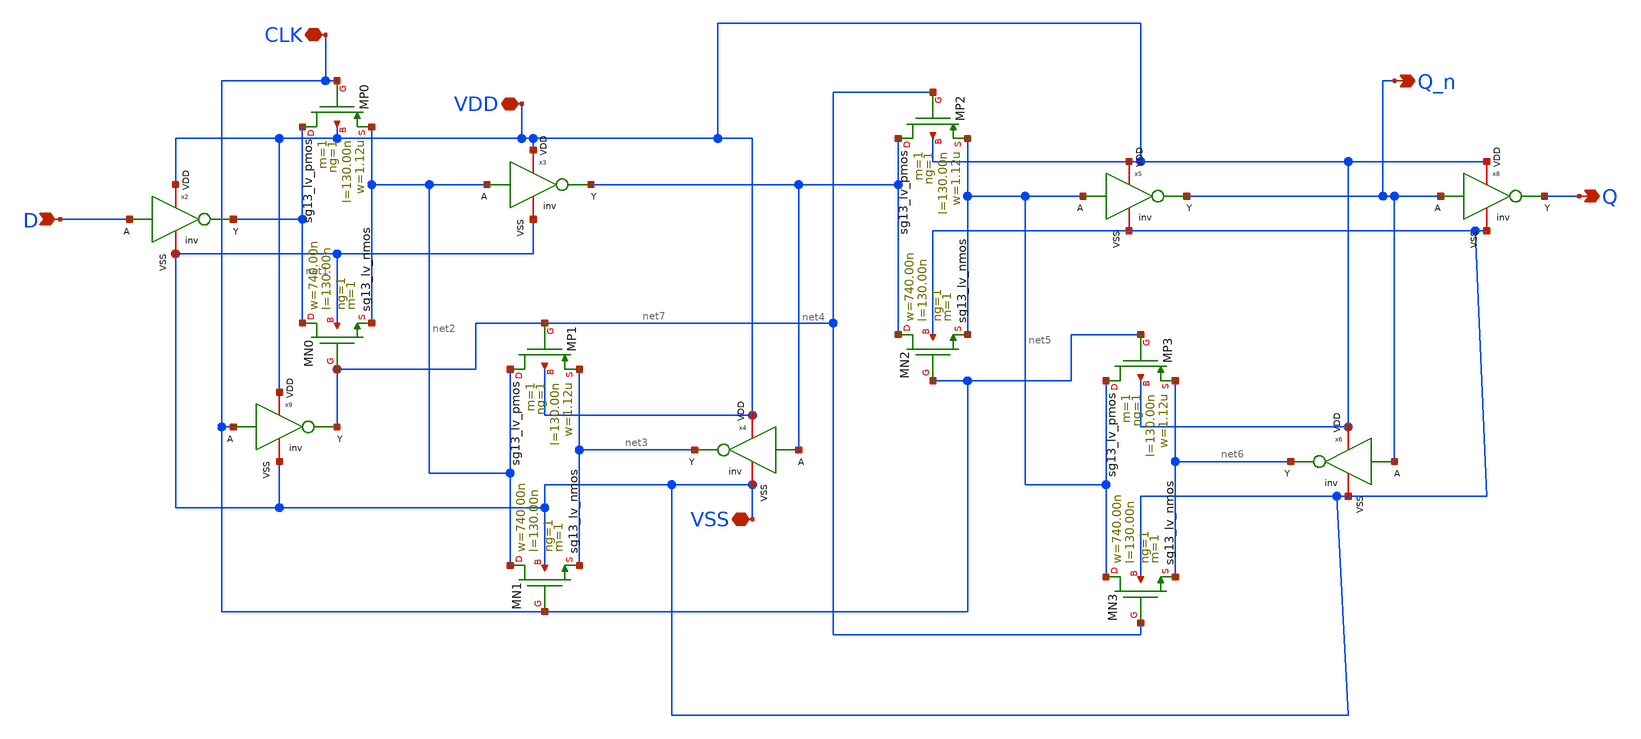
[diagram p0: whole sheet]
** sch_path: xschem/flipflopn.sch
**.subckt flipflopn D Q CLK VDD VSS Q_n
*.ipin D
*.opin Q
*.iopin CLK
*.iopin VDD
*.iopin VSS
*.opin Q_n
XMN0 net1 net7 net2 VSS sg13_lv_nmos w=740.00n l=130.00n ng=1 m=1 mm_ok=1
XMP0 net1 CLK net2 VDD sg13_lv_pmos w=1.12u l=130.00n ng=1 m=1 mm_ok=1
XMN1 net2 CLK net3 VSS sg13_lv_nmos w=740.00n l=130.00n ng=1 m=1 mm_ok=1
XMP1 net2 net7 net3 VDD sg13_lv_pmos w=1.12u l=130.00n ng=1 m=1 mm_ok=1
x2 VDD net1 D VSS inv
x3 VDD net4 net2 VSS inv
x4 VDD net3 net4 VSS inv
XMN2 net4 CLK net5 VSS sg13_lv_nmos w=740.00n l=130.00n ng=1 m=1 mm_ok=1
XMP2 net4 net7 net5 VDD sg13_lv_pmos w=1.12u l=130.00n ng=1 m=1 mm_ok=1
XMN3 net5 net7 net6 VSS sg13_lv_nmos w=740.00n l=130.00n ng=1 m=1 mm_ok=1
XMP3 net5 CLK net6 VDD sg13_lv_pmos w=1.12u l=130.00n ng=1 m=1 mm_ok=1
x5 VDD Q_n net5 VSS inv
x6 VDD net6 Q_n VSS inv
x8 VDD Q Q_n VSS inv
x9 VDD net7 CLK VSS inv
**.ends
.end
